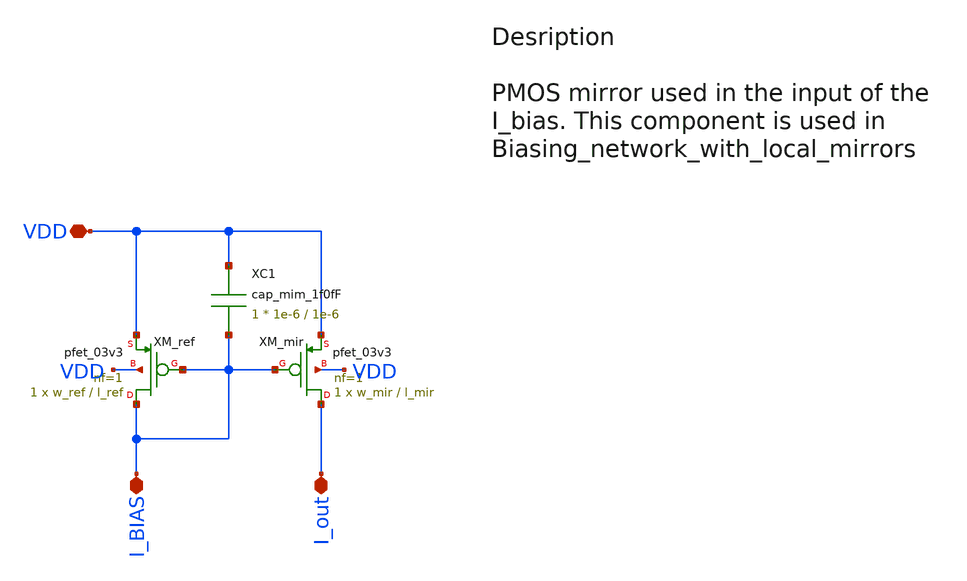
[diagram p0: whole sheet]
** sch_path: src/python/Cmirror_with_decap/Local_mirror_pmos.sch
**.subckt Local_mirror_pmos I_BIAS VDD I_out
*.iopin I_BIAS
*.iopin VDD
*.iopin I_out
XC1 VDD I_BIAS cap_mim_1f0fF c_width=1e-6 c_length=1e-6 m=1
XM_ref I_BIAS I_BIAS VDD VDD pfet_03v3 L=l_ref W=w_ref nf=1 ad='int((nf+1)/2) * W/nf * 0.18u' as='int((nf+2)/2) * W/nf * 0.18u'
+ pd='2*int((nf+1)/2) * (W/nf + 0.18u)' ps='2*int((nf+2)/2) * (W/nf + 0.18u)' nrd='0.18u / W' nrs='0.18u / W'
+ sa=0 sb=0 sd=0 m=1
XM_mir I_out I_BIAS VDD VDD pfet_03v3 L=l_mir W=w_mir nf=1 ad='int((nf+1)/2) * W/nf * 0.18u' as='int((nf+2)/2) * W/nf * 0.18u'
+ pd='2*int((nf+1)/2) * (W/nf + 0.18u)' ps='2*int((nf+2)/2) * (W/nf + 0.18u)' nrd='0.18u / W' nrs='0.18u / W'
+ sa=0 sb=0 sd=0 m=1
**** begin user architecture code

.include $::180MCU_MODELS/design.ngspice
.lib $::180MCU_MODELS/sm141064.ngspice typical
.lib $::180MCU_MODELS/sm141064.ngspice cap_mim
.lib $::180MCU_MODELS/sm141064.ngspice res_typical




* let sets vectors to a plot, while set sets a variable, globally accessible in .control
.control

    * Set frequency and amplitude variables to proper values from within the control sequence
    save all

    op
    show

    write Biasing_network_sim.raw

    set appendwrite

    * Transient analysis to observe mixing operation
    tran 1p 10n


    write Biasing_network_sim.raw

.endc


**** end user architecture code
**.ends
.end
